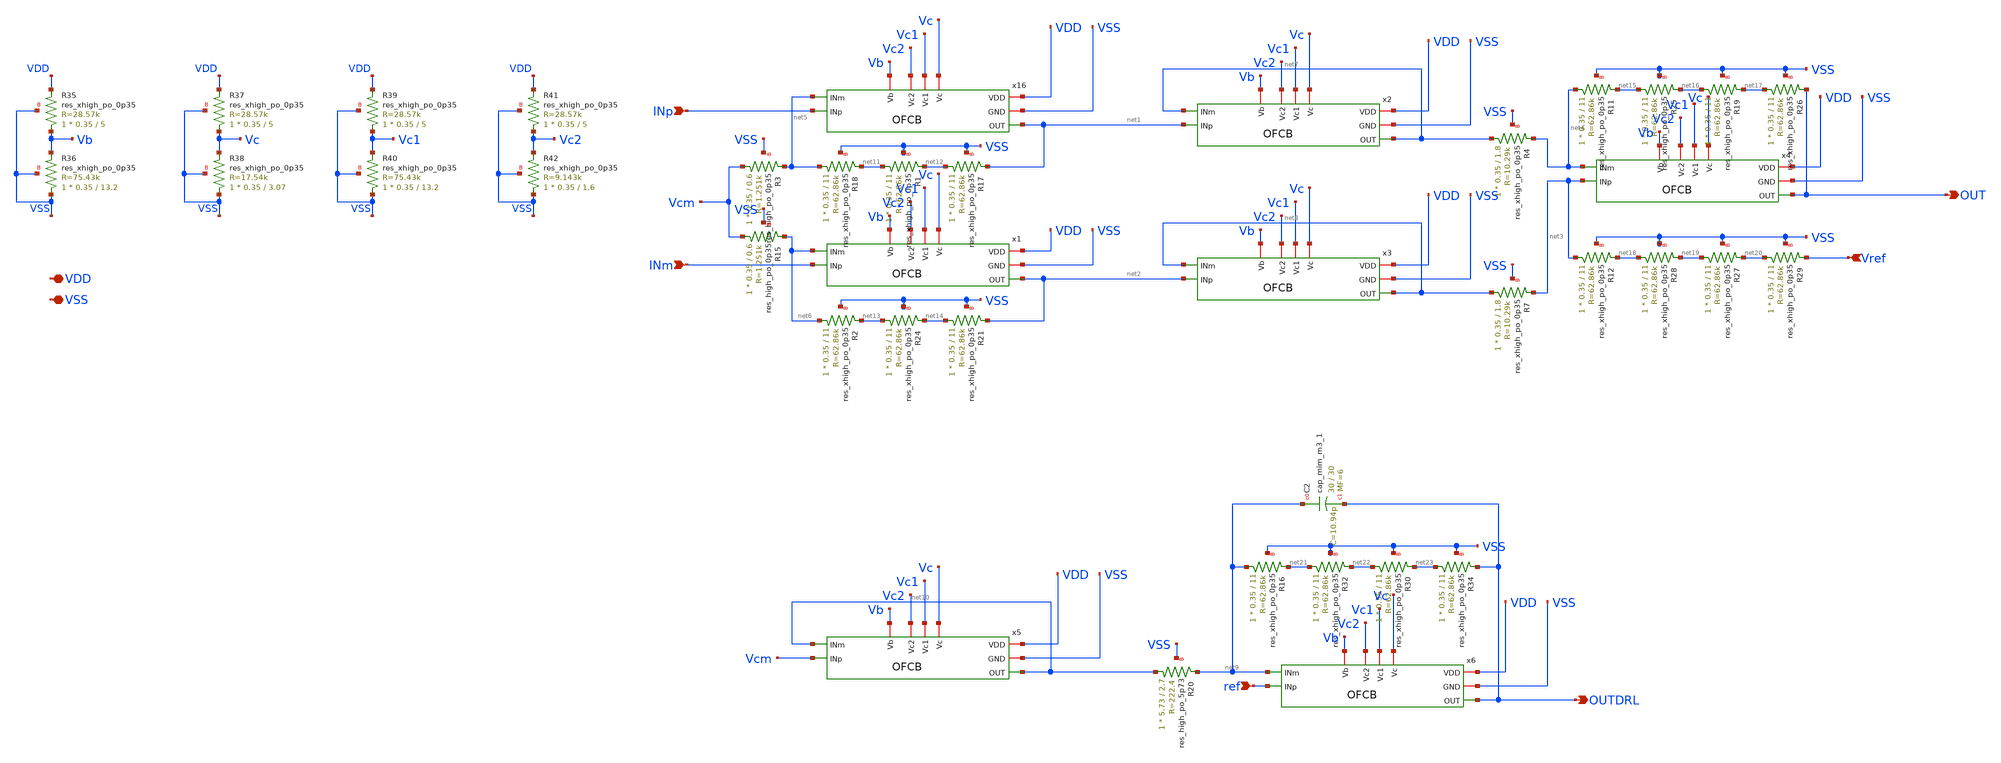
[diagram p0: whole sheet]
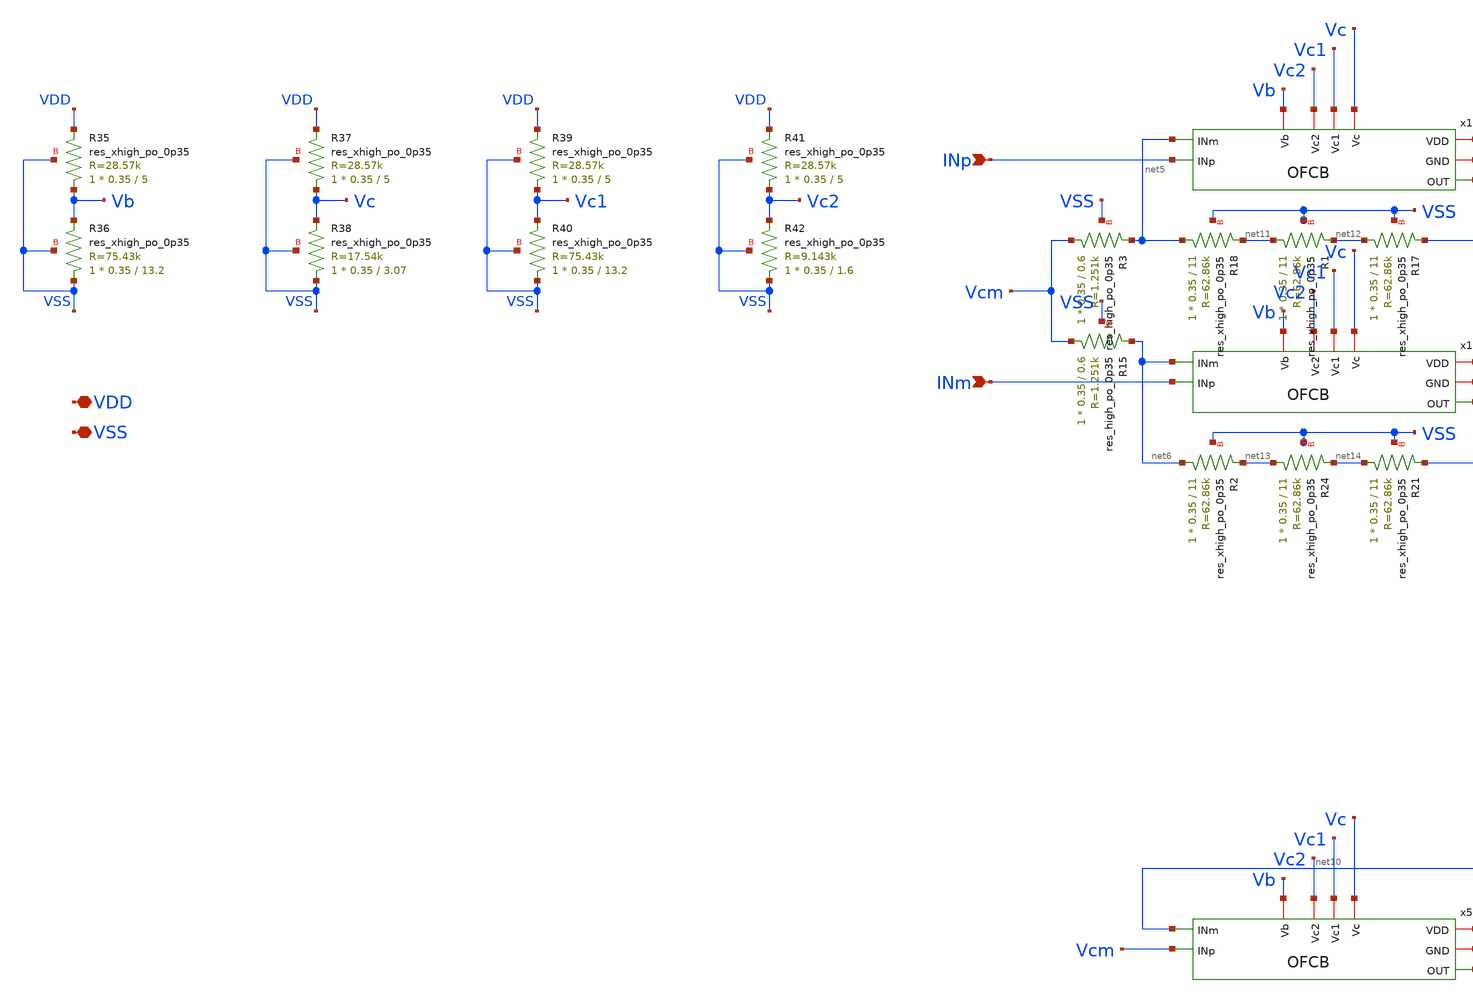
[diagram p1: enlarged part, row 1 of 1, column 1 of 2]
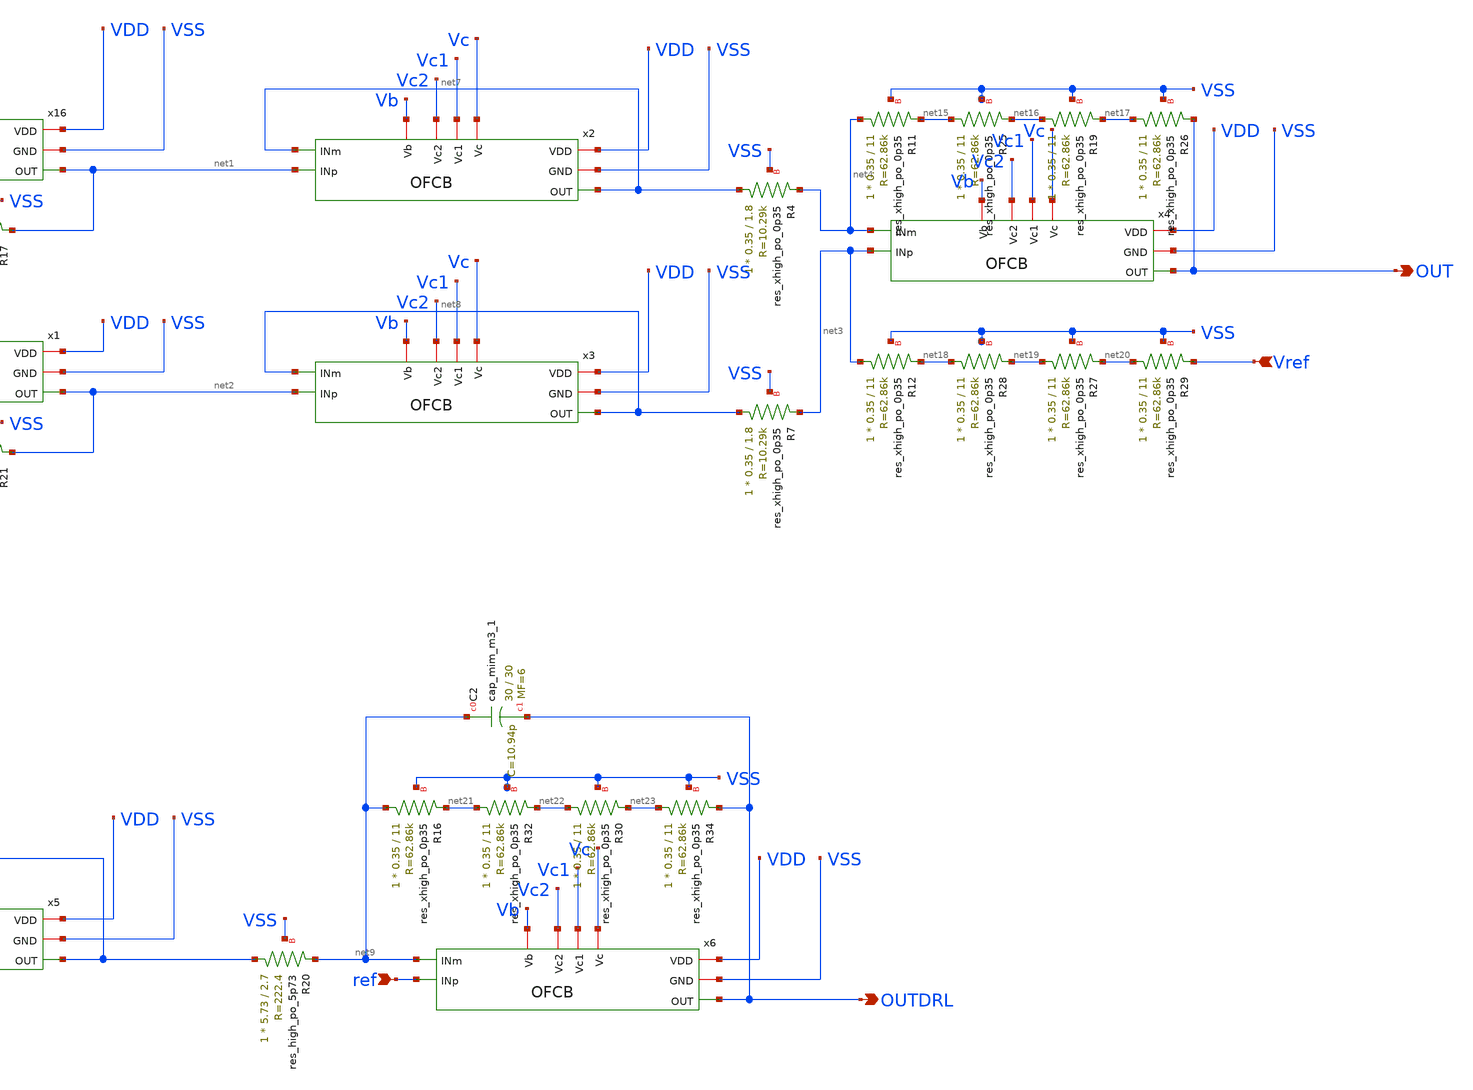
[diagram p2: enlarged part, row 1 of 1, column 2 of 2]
** sch_path: xschem/ecgF.sch
**.subckt ecgF INp INm OUT Vref OUTDRL ref VDD VSS
*.ipin INp
*.ipin INm
*.opin OUT
*.ipin Vref
*.opin OUTDRL
*.ipin ref
*.iopin VDD
*.iopin VSS
XR3 Vcm net5 VSS sky130_fd_pr__res_high_po_0p35 L=0.6 mult=1 m=1
XR15 Vcm net6 VSS sky130_fd_pr__res_high_po_0p35 L=0.6 mult=1 m=1
XR18 net5 net11 VSS sky130_fd_pr__res_xhigh_po_0p35 L=11 mult=1 m=1
XR20 net10 net9 VSS sky130_fd_pr__res_high_po_5p73 L=2.7 mult=1 m=1
XR17 net12 net1 VSS sky130_fd_pr__res_xhigh_po_0p35 L=11 mult=1 m=1
XR1 net11 net12 VSS sky130_fd_pr__res_xhigh_po_0p35 L=11 mult=1 m=1
XR2 net6 net13 VSS sky130_fd_pr__res_xhigh_po_0p35 L=11 mult=1 m=1
XR21 net14 net2 VSS sky130_fd_pr__res_xhigh_po_0p35 L=11 mult=1 m=1
XR24 net13 net14 VSS sky130_fd_pr__res_xhigh_po_0p35 L=11 mult=1 m=1
XR4 net7 net4 VSS sky130_fd_pr__res_xhigh_po_0p35 L=1.8 mult=1 m=1
XR7 net8 net3 VSS sky130_fd_pr__res_xhigh_po_0p35 L=1.8 mult=1 m=1
XR11 net4 net15 VSS sky130_fd_pr__res_xhigh_po_0p35 L=11 mult=1 m=1
XR19 net16 net17 VSS sky130_fd_pr__res_xhigh_po_0p35 L=11 mult=1 m=1
XR25 net15 net16 VSS sky130_fd_pr__res_xhigh_po_0p35 L=11 mult=1 m=1
XR26 net17 OUT VSS sky130_fd_pr__res_xhigh_po_0p35 L=11 mult=1 m=1
XR12 net3 net18 VSS sky130_fd_pr__res_xhigh_po_0p35 L=11 mult=1 m=1
XR27 net19 net20 VSS sky130_fd_pr__res_xhigh_po_0p35 L=11 mult=1 m=1
XR28 net18 net19 VSS sky130_fd_pr__res_xhigh_po_0p35 L=11 mult=1 m=1
XR29 net20 Vref VSS sky130_fd_pr__res_xhigh_po_0p35 L=11 mult=1 m=1
XC2 net9 OUTDRL sky130_fd_pr__cap_mim_m3_1 W=30 L=30 MF=6 m=6
XR16 net9 net21 VSS sky130_fd_pr__res_xhigh_po_0p35 L=11 mult=1 m=1
XR30 net22 net23 VSS sky130_fd_pr__res_xhigh_po_0p35 L=11 mult=1 m=1
XR32 net21 net22 VSS sky130_fd_pr__res_xhigh_po_0p35 L=11 mult=1 m=1
XR34 net23 OUTDRL VSS sky130_fd_pr__res_xhigh_po_0p35 L=11 mult=1 m=1
x16 Vb VDD VSS Vc2 net1 INp net5 Vc1 Vc OFCB
x1 Vb VDD VSS Vc2 net2 INm net6 Vc1 Vc OFCB
x2 Vb VDD VSS Vc2 net7 net1 net7 Vc1 Vc OFCB
x3 Vb VDD VSS Vc2 net8 net2 net8 Vc1 Vc OFCB
x4 Vb VDD VSS Vc2 OUT net3 net4 Vc1 Vc OFCB
x5 Vb VDD VSS Vc2 net10 Vcm net10 Vc1 Vc OFCB
x6 Vb VDD VSS Vc2 OUTDRL ref net9 Vc1 Vc OFCB
XR35 Vb VDD VSS sky130_fd_pr__res_xhigh_po_0p35 L=5 mult=1 m=1
XR36 VSS Vb VSS sky130_fd_pr__res_xhigh_po_0p35 L=13.2 mult=1 m=1
XR37 Vc VDD VSS sky130_fd_pr__res_xhigh_po_0p35 L=5 mult=1 m=1
XR38 VSS Vc VSS sky130_fd_pr__res_xhigh_po_0p35 L=3.07 mult=1 m=1
XR39 Vc1 VDD VSS sky130_fd_pr__res_xhigh_po_0p35 L=5 mult=1 m=1
XR40 VSS Vc1 VSS sky130_fd_pr__res_xhigh_po_0p35 L=13.2 mult=1 m=1
XR41 Vc2 VDD VSS sky130_fd_pr__res_xhigh_po_0p35 L=5 mult=1 m=1
XR42 VSS Vc2 VSS sky130_fd_pr__res_xhigh_po_0p35 L=1.6 mult=1 m=1
**.ends

* expanding   symbol:  OFCB.sym # of pins=9
** sym_path: xschem/OFCB.sym
** sch_path: xschem/OFCB.sch
.subckt OFCB Vb VDD GND Vc2 OUT INp INm Vc1 Vc
*.iopin VDD
*.iopin GND
*.opin OUT
*.ipin INp
*.ipin INm
*.iopin Vc2
*.iopin Vc1
*.iopin Vc
*.iopin Vb
XM11 S Vb VDD VDD sky130_fd_pr__pfet_01v8_lvt L=1 W=60 nf=6 ad='int((nf+1)/2) * W/nf * 0.29' as='int((nf+2)/2) * W/nf * 0.29'
+ pd='2*int((nf+1)/2) * (W/nf + 0.29)' ps='2*int((nf+2)/2) * (W/nf + 0.29)' nrd='0.29 / W' nrs='0.29 / W'
+ sa=0 sb=0 sd=0 mult=2 m=2
XM1 D1 INp S S sky130_fd_pr__pfet_01v8_lvt L=10 W=25 nf=2 ad='int((nf+1)/2) * W/nf * 0.29' as='int((nf+2)/2) * W/nf * 0.29'
+ pd='2*int((nf+1)/2) * (W/nf + 0.29)' ps='2*int((nf+2)/2) * (W/nf + 0.29)' nrd='0.29 / W' nrs='0.29 / W'
+ sa=0 sb=0 sd=0 mult=2 m=2
XM2 D2 INm S S sky130_fd_pr__pfet_01v8_lvt L=10 W=25 nf=2 ad='int((nf+1)/2) * W/nf * 0.29' as='int((nf+2)/2) * W/nf * 0.29'
+ pd='2*int((nf+1)/2) * (W/nf + 0.29)' ps='2*int((nf+2)/2) * (W/nf + 0.29)' nrd='0.29 / W' nrs='0.29 / W'
+ sa=0 sb=0 sd=0 mult=2 m=2
XM3 OUT Vc1 D2 GND sky130_fd_pr__nfet_01v8_lvt L=1 W=4 nf=1 ad='int((nf+1)/2) * W/nf * 0.29' as='int((nf+2)/2) * W/nf * 0.29'
+ pd='2*int((nf+1)/2) * (W/nf + 0.29)' ps='2*int((nf+2)/2) * (W/nf + 0.29)' nrd='0.29 / W' nrs='0.29 / W'
+ sa=0 sb=0 sd=0 mult=1 m=1
XM4 D2 Vc GND GND sky130_fd_pr__nfet_01v8_lvt L=1 W=2.8 nf=1 ad='int((nf+1)/2) * W/nf * 0.29' as='int((nf+2)/2) * W/nf * 0.29'
+ pd='2*int((nf+1)/2) * (W/nf + 0.29)' ps='2*int((nf+2)/2) * (W/nf + 0.29)' nrd='0.29 / W' nrs='0.29 / W'
+ sa=0 sb=0 sd=0 mult=1 m=1
XM5 D1 Vc GND GND sky130_fd_pr__nfet_01v8_lvt L=1 W=2.8 nf=1 ad='int((nf+1)/2) * W/nf * 0.29' as='int((nf+2)/2) * W/nf * 0.29'
+ pd='2*int((nf+1)/2) * (W/nf + 0.29)' ps='2*int((nf+2)/2) * (W/nf + 0.29)' nrd='0.29 / W' nrs='0.29 / W'
+ sa=0 sb=0 sd=0 mult=1 m=1
XM6 G Vc1 D1 GND sky130_fd_pr__nfet_01v8_lvt L=1 W=4 nf=1 ad='int((nf+1)/2) * W/nf * 0.29' as='int((nf+2)/2) * W/nf * 0.29'
+ pd='2*int((nf+1)/2) * (W/nf + 0.29)' ps='2*int((nf+2)/2) * (W/nf + 0.29)' nrd='0.29 / W' nrs='0.29 / W'
+ sa=0 sb=0 sd=0 mult=1 m=1
XM7 G Vc2 D9 D9 sky130_fd_pr__pfet_01v8_lvt L=2.23 W=4 nf=1 ad='int((nf+1)/2) * W/nf * 0.29' as='int((nf+2)/2) * W/nf * 0.29'
+ pd='2*int((nf+1)/2) * (W/nf + 0.29)' ps='2*int((nf+2)/2) * (W/nf + 0.29)' nrd='0.29 / W' nrs='0.29 / W'
+ sa=0 sb=0 sd=0 mult=1 m=1
XM9 D9 G VDD VDD sky130_fd_pr__pfet_01v8_lvt L=2.23 W=3.85 nf=1 ad='int((nf+1)/2) * W/nf * 0.29' as='int((nf+2)/2) * W/nf * 0.29'
+ pd='2*int((nf+1)/2) * (W/nf + 0.29)' ps='2*int((nf+2)/2) * (W/nf + 0.29)' nrd='0.29 / W' nrs='0.29 / W'
+ sa=0 sb=0 sd=0 mult=1 m=1
XM8 D10 G VDD VDD sky130_fd_pr__pfet_01v8_lvt L=2.23 W=3.85 nf=1 ad='int((nf+1)/2) * W/nf * 0.29' as='int((nf+2)/2) * W/nf * 0.29'
+ pd='2*int((nf+1)/2) * (W/nf + 0.29)' ps='2*int((nf+2)/2) * (W/nf + 0.29)' nrd='0.29 / W' nrs='0.29 / W'
+ sa=0 sb=0 sd=0 mult=1 m=1
XM10 OUT Vc2 D10 D10 sky130_fd_pr__pfet_01v8_lvt L=2.23 W=4 nf=1 ad='int((nf+1)/2) * W/nf * 0.29' as='int((nf+2)/2) * W/nf * 0.29'
+ pd='2*int((nf+1)/2) * (W/nf + 0.29)' ps='2*int((nf+2)/2) * (W/nf + 0.29)' nrd='0.29 / W' nrs='0.29 / W'
+ sa=0 sb=0 sd=0 mult=1 m=1
XC1 OUT D1 sky130_fd_pr__cap_mim_m3_1 W=22.4 L=22.4 MF=2 m=2
.ends

.end
